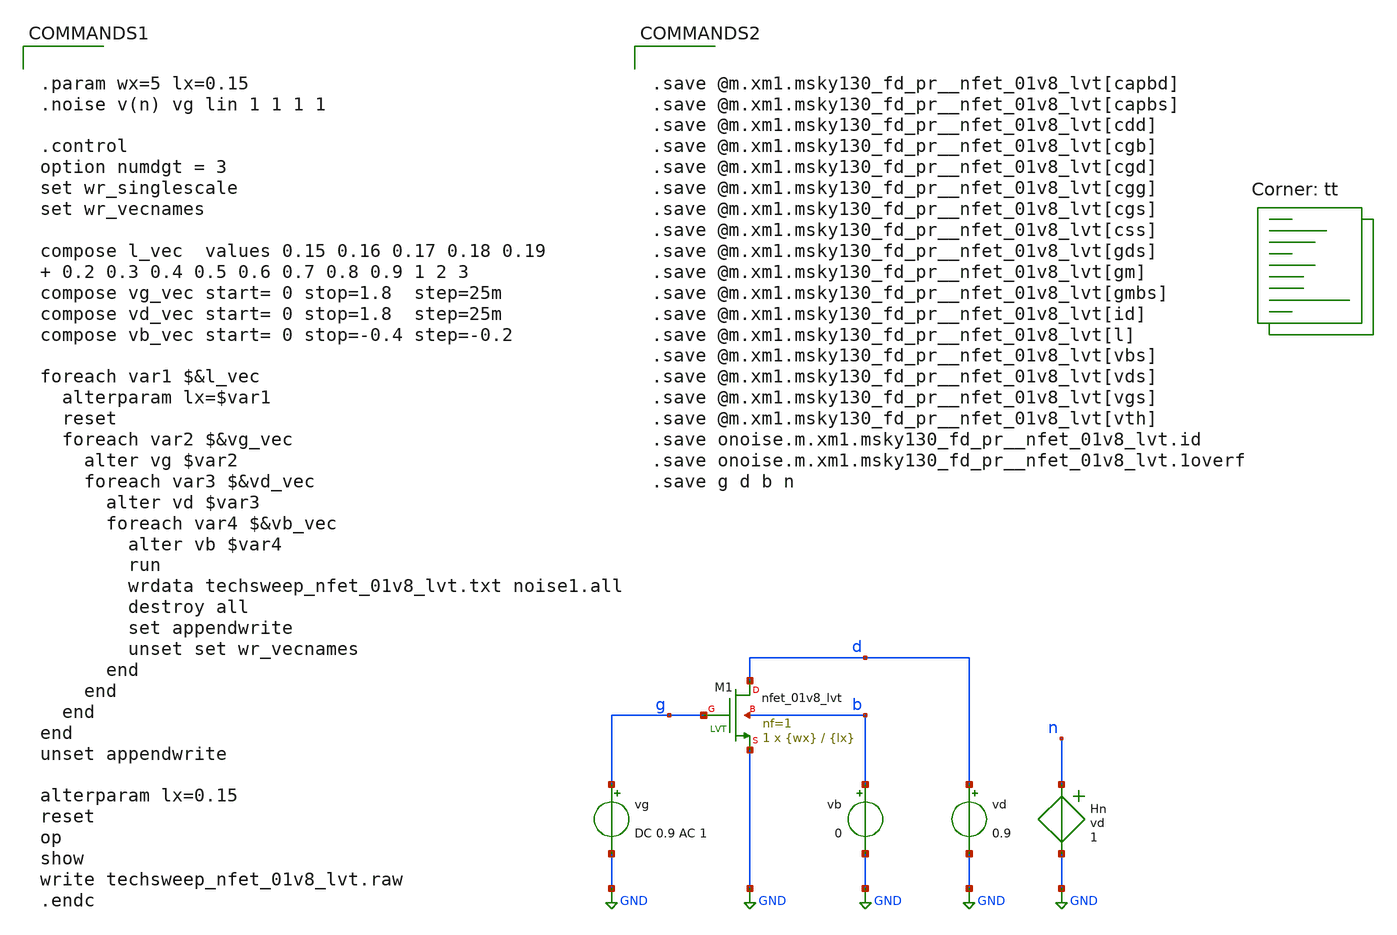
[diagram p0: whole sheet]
** sch_path: ISSCC25/submitted_notebooks/analog_vibes/OTA/scripts/techsweep/techsweep_nfet_01v8_lvt.sch
**.subckt techsweep_nfet_01v8_lvt
vg g GND DC 0.9 AC 1
vd d GND 0.9
vb b GND 0
XM1 d g GND b sky130_fd_pr__nfet_01v8_lvt L={lx} W={wx} nf=1 ad='int((nf+1)/2) * W/nf * 0.29' as='int((nf+2)/2) * W/nf * 0.29'
+ pd='2*int((nf+1)/2) * (W/nf + 0.29)' ps='2*int((nf+2)/2) * (W/nf + 0.29)' nrd='0.29 / W' nrs='0.29 / W'
+ sa=0 sb=0 sd=0 mult=1 m=1
Hn n GND vd 1
**** begin user architecture code


.param wx=5 lx=0.15
.noise v(n) vg lin 1 1 1 1

.control
option numdgt = 3
set wr_singlescale
set wr_vecnames

compose l_vec  values 0.15 0.16 0.17 0.18 0.19  0.2 0.3 0.4 0.5 0.6 0.7 0.8 0.9 1 2 3
compose vg_vec start= 0 stop=1.8  step=25m
compose vd_vec start= 0 stop=1.8  step=25m
compose vb_vec start= 0 stop=-0.4 step=-0.2

foreach var1 $&l_vec
  alterparam lx=$var1
  reset
  foreach var2 $&vg_vec
    alter vg $var2
    foreach var3 $&vd_vec
      alter vd $var3
      foreach var4 $&vb_vec
        alter vb $var4
        run
        wrdata techsweep_nfet_01v8_lvt.txt noise1.all
        destroy all
        set appendwrite
        unset set wr_vecnames
      end
    end
  end
end
unset appendwrite

alterparam lx=0.15
reset
op
show
write techsweep_nfet_01v8_lvt.raw
.endc


.lib $::SKYWATER_MODELS/sky130.lib.spice tt


.save @m.xm1.msky130_fd_pr__nfet_01v8_lvt[capbd]
.save @m.xm1.msky130_fd_pr__nfet_01v8_lvt[capbs]
.save @m.xm1.msky130_fd_pr__nfet_01v8_lvt[cdd]
.save @m.xm1.msky130_fd_pr__nfet_01v8_lvt[cgb]
.save @m.xm1.msky130_fd_pr__nfet_01v8_lvt[cgd]
.save @m.xm1.msky130_fd_pr__nfet_01v8_lvt[cgg]
.save @m.xm1.msky130_fd_pr__nfet_01v8_lvt[cgs]
.save @m.xm1.msky130_fd_pr__nfet_01v8_lvt[css]
.save @m.xm1.msky130_fd_pr__nfet_01v8_lvt[gds]
.save @m.xm1.msky130_fd_pr__nfet_01v8_lvt[gm]
.save @m.xm1.msky130_fd_pr__nfet_01v8_lvt[gmbs]
.save @m.xm1.msky130_fd_pr__nfet_01v8_lvt[id]
.save @m.xm1.msky130_fd_pr__nfet_01v8_lvt[l]
.save @m.xm1.msky130_fd_pr__nfet_01v8_lvt[vbs]
.save @m.xm1.msky130_fd_pr__nfet_01v8_lvt[vds]
.save @m.xm1.msky130_fd_pr__nfet_01v8_lvt[vgs]
.save @m.xm1.msky130_fd_pr__nfet_01v8_lvt[vth]
.save onoise.m.xm1.msky130_fd_pr__nfet_01v8_lvt.id
.save onoise.m.xm1.msky130_fd_pr__nfet_01v8_lvt.1overf
.save g d b n


**** end user architecture code
**.ends
.GLOBAL GND
.end
